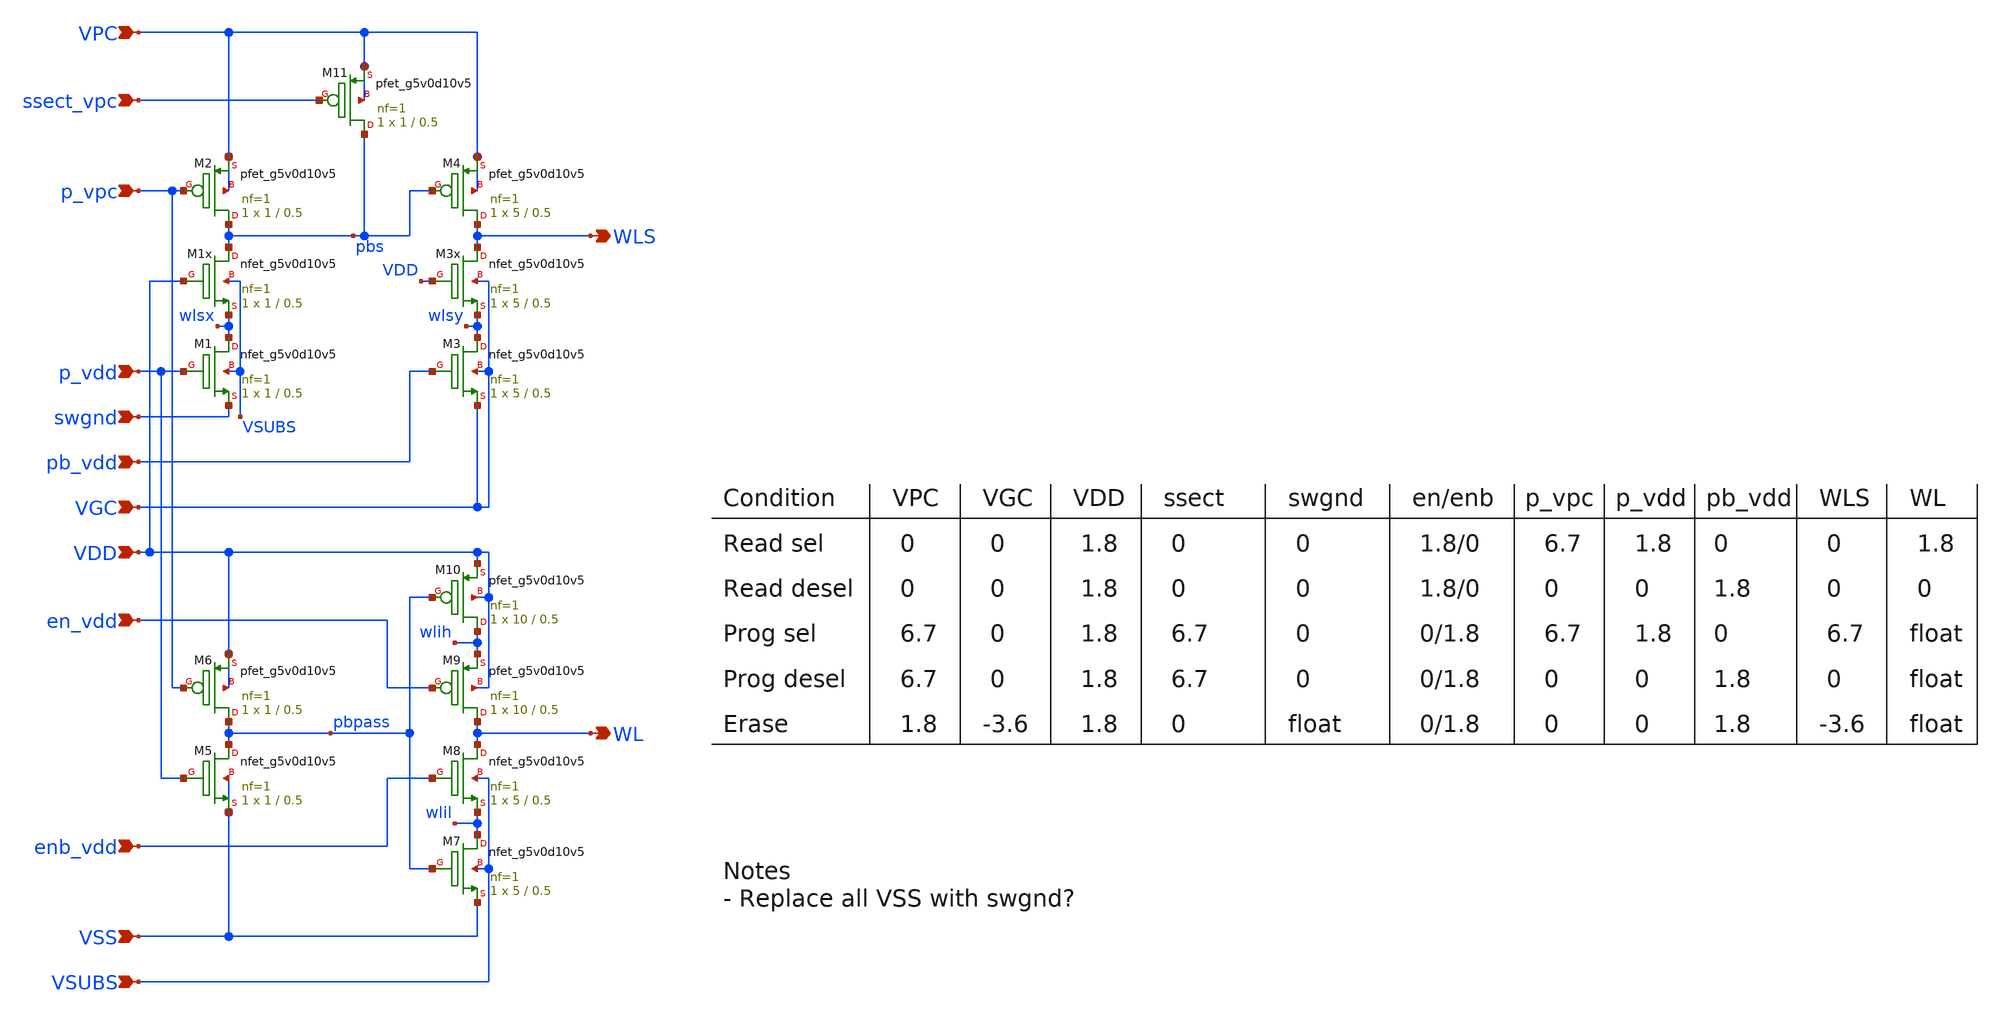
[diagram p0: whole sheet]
** sch_path: integrated/rowdv_2t_sonos/rowdv_2t.sch
**.subckt rowdv_2t p_vpc WLS swgnd VDD VSS en_vdd enb_vdd VGC VPC ssect_vpc WL VSUBS p_vdd pb_vdd
*.ipin p_vpc
*.opin WLS
*.ipin swgnd
*.ipin VDD
*.ipin VSS
*.ipin en_vdd
*.ipin enb_vdd
*.ipin VGC
*.ipin VPC
*.ipin ssect_vpc
*.opin WL
*.ipin VSUBS
*.ipin p_vdd
*.ipin pb_vdd
XM1 wlsx p_vdd swgnd VSUBS sky130_fd_pr__nfet_g5v0d10v5 L=0.5 W=1 nf=1 ad='int((nf+1)/2) * W/nf * 0.29'
+ as='int((nf+2)/2) * W/nf * 0.29' pd='2*int((nf+1)/2) * (W/nf + 0.29)' ps='2*int((nf+2)/2) * (W/nf + 0.29)'
+ nrd='0.29 / W' nrs='0.29 / W' sa=0 sb=0 sd=0 mult=1 m=1
XM2 pbs p_vpc VPC VPC sky130_fd_pr__pfet_g5v0d10v5 L=0.5 W=1 nf=1 ad='int((nf+1)/2) * W/nf * 0.29' as='int((nf+2)/2) * W/nf * 0.29'
+ pd='2*int((nf+1)/2) * (W/nf + 0.29)' ps='2*int((nf+2)/2) * (W/nf + 0.29)' nrd='0.29 / W' nrs='0.29 / W'
+ sa=0 sb=0 sd=0 mult=1 m=1
XM3 wlsy pb_vdd VGC VGC sky130_fd_pr__nfet_g5v0d10v5 L=0.5 W=5 nf=1 ad='int((nf+1)/2) * W/nf * 0.29'
+ as='int((nf+2)/2) * W/nf * 0.29' pd='2*int((nf+1)/2) * (W/nf + 0.29)' ps='2*int((nf+2)/2) * (W/nf + 0.29)'
+ nrd='0.29 / W' nrs='0.29 / W' sa=0 sb=0 sd=0 mult=1 m=1
XM4 WLS pbs VPC VPC sky130_fd_pr__pfet_g5v0d10v5 L=0.5 W=5 nf=1 ad='int((nf+1)/2) * W/nf * 0.29' as='int((nf+2)/2) * W/nf * 0.29'
+ pd='2*int((nf+1)/2) * (W/nf + 0.29)' ps='2*int((nf+2)/2) * (W/nf + 0.29)' nrd='0.29 / W' nrs='0.29 / W'
+ sa=0 sb=0 sd=0 mult=1 m=1
XM6 pbpass p_vpc VDD VDD sky130_fd_pr__pfet_g5v0d10v5 L=0.5 W=1 nf=1 ad='int((nf+1)/2) * W/nf * 0.29'
+ as='int((nf+2)/2) * W/nf * 0.29' pd='2*int((nf+1)/2) * (W/nf + 0.29)' ps='2*int((nf+2)/2) * (W/nf + 0.29)'
+ nrd='0.29 / W' nrs='0.29 / W' sa=0 sb=0 sd=0 mult=1 m=1
XM7 wlil pbpass VSS VSUBS sky130_fd_pr__nfet_g5v0d10v5 L=0.5 W=5 nf=1 ad='int((nf+1)/2) * W/nf * 0.29'
+ as='int((nf+2)/2) * W/nf * 0.29' pd='2*int((nf+1)/2) * (W/nf + 0.29)' ps='2*int((nf+2)/2) * (W/nf + 0.29)'
+ nrd='0.29 / W' nrs='0.29 / W' sa=0 sb=0 sd=0 mult=1 m=1
XM9 WL en_vdd wlih VDD sky130_fd_pr__pfet_g5v0d10v5 L=0.5 W=10 nf=1 ad='int((nf+1)/2) * W/nf * 0.29'
+ as='int((nf+2)/2) * W/nf * 0.29' pd='2*int((nf+1)/2) * (W/nf + 0.29)' ps='2*int((nf+2)/2) * (W/nf + 0.29)'
+ nrd='0.29 / W' nrs='0.29 / W' sa=0 sb=0 sd=0 mult=1 m=1
XM8 WL enb_vdd wlil VSUBS sky130_fd_pr__nfet_g5v0d10v5 L=0.5 W=5 nf=1 ad='int((nf+1)/2) * W/nf * 0.29'
+ as='int((nf+2)/2) * W/nf * 0.29' pd='2*int((nf+1)/2) * (W/nf + 0.29)' ps='2*int((nf+2)/2) * (W/nf + 0.29)'
+ nrd='0.29 / W' nrs='0.29 / W' sa=0 sb=0 sd=0 mult=1 m=1
XM10 wlih pbpass VDD VDD sky130_fd_pr__pfet_g5v0d10v5 L=0.5 W=10 nf=1 ad='int((nf+1)/2) * W/nf * 0.29'
+ as='int((nf+2)/2) * W/nf * 0.29' pd='2*int((nf+1)/2) * (W/nf + 0.29)' ps='2*int((nf+2)/2) * (W/nf + 0.29)'
+ nrd='0.29 / W' nrs='0.29 / W' sa=0 sb=0 sd=0 mult=1 m=1
XM11 pbs ssect_vpc VPC VPC sky130_fd_pr__pfet_g5v0d10v5 L=0.5 W=1 nf=1 ad='int((nf+1)/2) * W/nf * 0.29'
+ as='int((nf+2)/2) * W/nf * 0.29' pd='2*int((nf+1)/2) * (W/nf + 0.29)' ps='2*int((nf+2)/2) * (W/nf + 0.29)'
+ nrd='0.29 / W' nrs='0.29 / W' sa=0 sb=0 sd=0 mult=1 m=1
XM5 pbpass p_vdd VSS VSS sky130_fd_pr__nfet_g5v0d10v5 L=0.5 W=1 nf=1 ad='int((nf+1)/2) * W/nf * 0.29'
+ as='int((nf+2)/2) * W/nf * 0.29' pd='2*int((nf+1)/2) * (W/nf + 0.29)' ps='2*int((nf+2)/2) * (W/nf + 0.29)'
+ nrd='0.29 / W' nrs='0.29 / W' sa=0 sb=0 sd=0 mult=1 m=1
XM1x pbs VDD wlsx VSUBS sky130_fd_pr__nfet_g5v0d10v5 L=0.5 W=1 nf=1 ad='int((nf+1)/2) * W/nf * 0.29'
+ as='int((nf+2)/2) * W/nf * 0.29' pd='2*int((nf+1)/2) * (W/nf + 0.29)' ps='2*int((nf+2)/2) * (W/nf + 0.29)'
+ nrd='0.29 / W' nrs='0.29 / W' sa=0 sb=0 sd=0 mult=1 m=1
XM3x WLS VDD wlsy VGC sky130_fd_pr__nfet_g5v0d10v5 L=0.5 W=5 nf=1 ad='int((nf+1)/2) * W/nf * 0.29' as='int((nf+2)/2) * W/nf * 0.29'
+ pd='2*int((nf+1)/2) * (W/nf + 0.29)' ps='2*int((nf+2)/2) * (W/nf + 0.29)' nrd='0.29 / W' nrs='0.29 / W'
+ sa=0 sb=0 sd=0 mult=1 m=1
**.ends
.end
